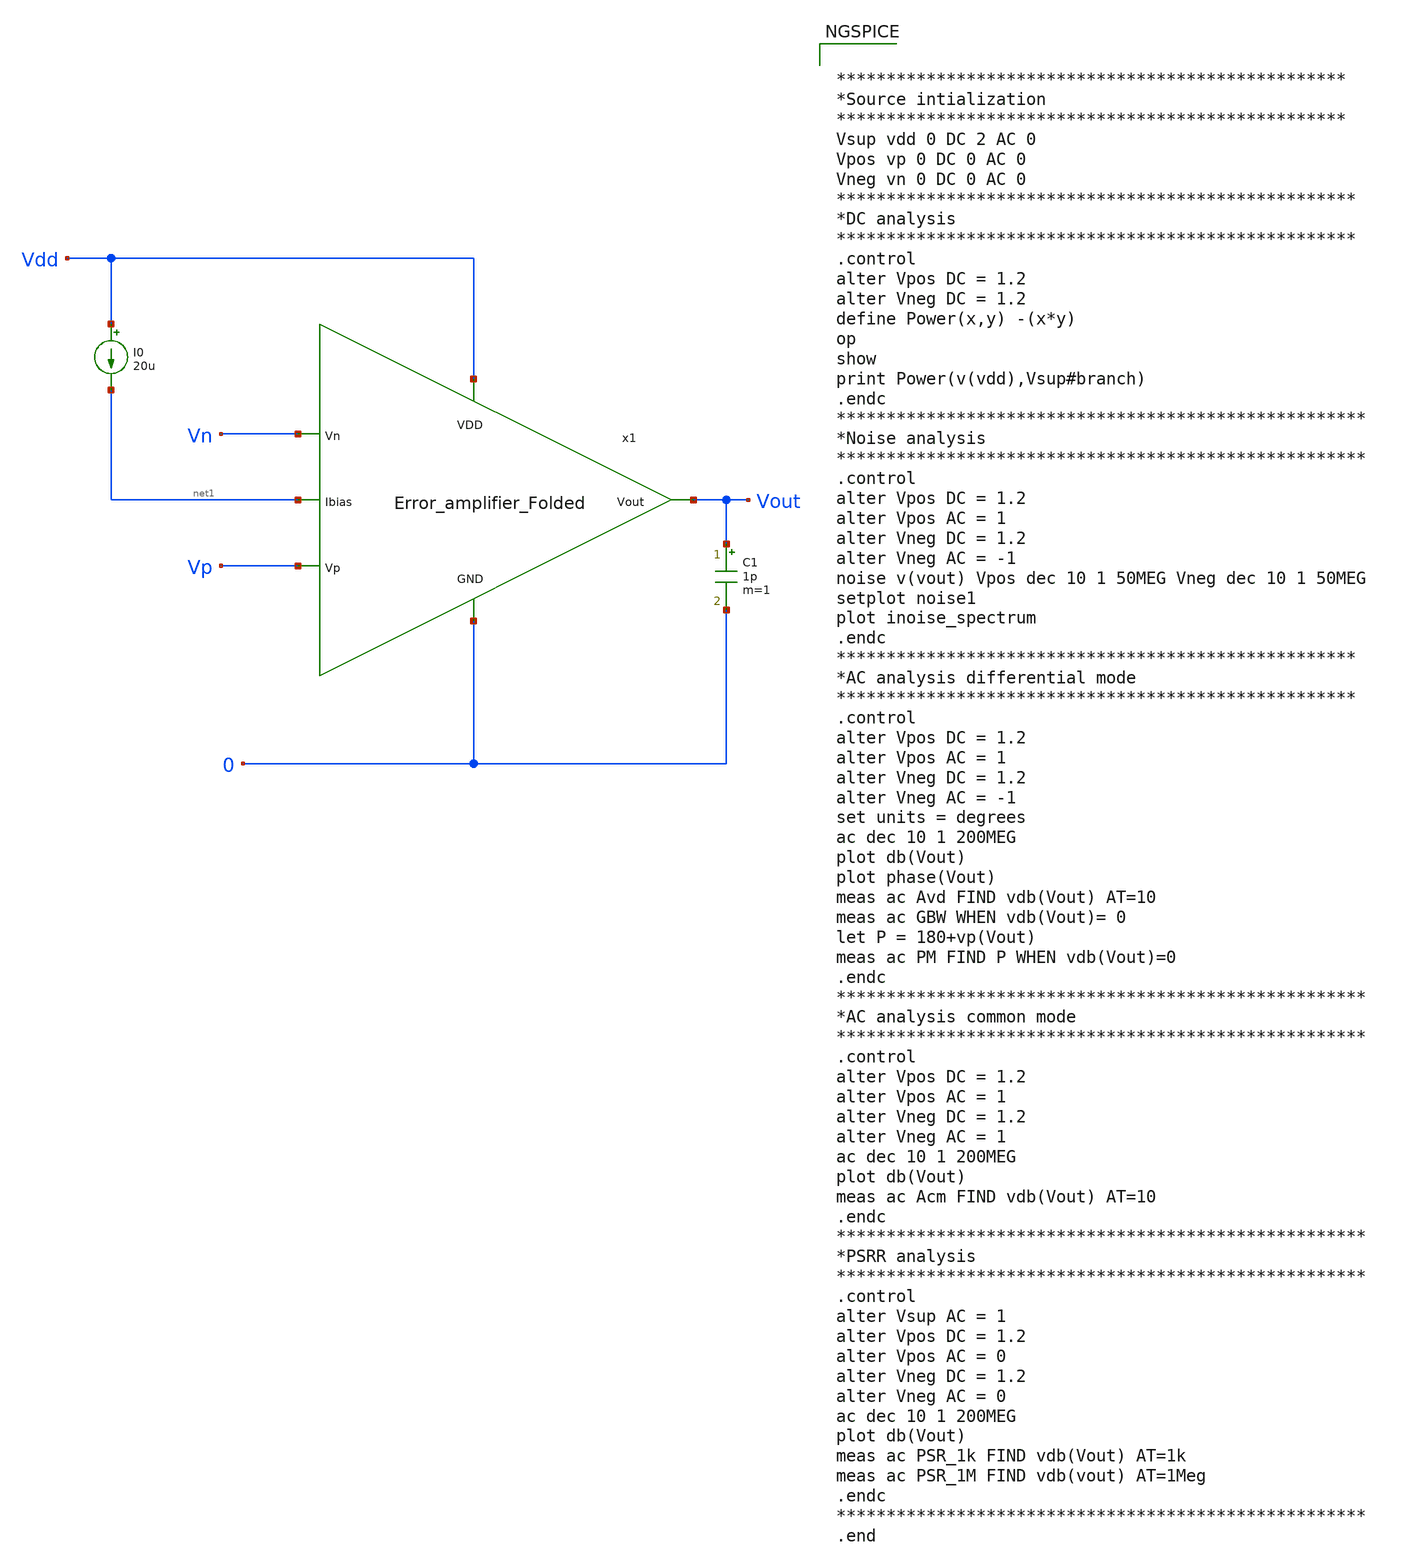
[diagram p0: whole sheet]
** sch_path: Analog_Blocks/OTA/Testbench/Folded_Cascode/Transistor5v/Error_amplifier_Folded_TB.sch
**.subckt Error_amplifier_Folded_TB
I0 Vdd net1 20u
C1 Vout 0 1p m=1
x1 Vdd Vout Vp Vn net1 0 Error_amplifier_Folded
**** begin user architecture code


***************************************************
*Source intialization
***************************************************
Vsup vdd 0 DC 2 AC 0
Vpos vp 0 DC 0 AC 0
Vneg vn 0 DC 0 AC 0
****************************************************
*DC analysis
****************************************************
.control
alter Vpos DC = 1.2
alter Vneg DC = 1.2
define Power(x,y) -(x*y)
op
show
print Power(v(vdd),Vsup#branch)
.endc
*****************************************************
*Noise analysis
*****************************************************
.control
alter Vpos DC = 1.2
alter Vpos AC = 1
alter Vneg DC = 1.2
alter Vneg AC = -1
noise v(vout) Vpos dec 10 1 50MEG Vneg dec 10 1 50MEG
setplot noise1
plot inoise_spectrum
.endc
****************************************************
*AC analysis differential mode
****************************************************
.control
alter Vpos DC = 1.2
alter Vpos AC = 1
alter Vneg DC = 1.2
alter Vneg AC = -1
set units = degrees
ac dec 10 1 200MEG
plot db(Vout)
plot phase(Vout)
meas ac Avd FIND vdb(Vout) AT=10
meas ac GBW WHEN vdb(Vout)= 0
let P = 180+vp(Vout)
meas ac PM FIND P WHEN vdb(Vout)=0
.endc
*****************************************************
*AC analysis common mode
*****************************************************
.control
alter Vpos DC = 1.2
alter Vpos AC = 1
alter Vneg DC = 1.2
alter Vneg AC = 1
ac dec 10 1 200MEG
plot db(Vout)
meas ac Acm FIND vdb(Vout) AT=10
.endc
*****************************************************
*PSRR analysis
*****************************************************
.control
alter Vsup AC = 1
alter Vpos DC = 1.2
alter Vpos AC = 0
alter Vneg DC = 1.2
alter Vneg AC = 0
ac dec 10 1 200MEG
plot db(Vout)
meas ac PSR_1k FIND vdb(Vout) AT=1k
meas ac PSR_1M FIND vdb(vout) AT=1Meg
.endc
*****************************************************
.end




.param mc_mm_switch=0
.param mc_pr_switch=0
.include ~/mabrains/Analog_blocks/models/sky130A/libs.ref/sky130_fd_pr/spice/sky130_fd_pr__nfet_01v8__tt.corner.spice
.include ~/mabrains/Analog_blocks/models/sky130A/libs.ref/sky130_fd_pr/spice/sky130_fd_pr__nfet_01v8_lvt__tt.corner.spice
.include ~/mabrains/Analog_blocks/models/sky130A/libs.ref/sky130_fd_pr/spice/sky130_fd_pr__pfet_01v8__tt.corner.spice
.include ~/mabrains/Analog_blocks/models/sky130A/libs.ref/sky130_fd_pr/spice/sky130_fd_pr__nfet_03v3_nvt__tt.corner.spice
.include ~/mabrains/Analog_blocks/models/sky130A/libs.ref/sky130_fd_pr/spice/sky130_fd_pr__nfet_05v0_nvt__tt.corner.spice
.include ~/mabrains/Analog_blocks/models/sky130A/libs.ref/sky130_fd_pr/spice/sky130_fd_pr__esd_nfet_01v8__tt.corner.spice
.include ~/mabrains/Analog_blocks/models/sky130A/libs.ref/sky130_fd_pr/spice/sky130_fd_pr__pfet_01v8_lvt__tt.corner.spice
.include ~/mabrains/Analog_blocks/models/sky130A/libs.ref/sky130_fd_pr/spice/sky130_fd_pr__pfet_01v8_hvt__tt.corner.spice
.include ~/mabrains/Analog_blocks/models/sky130A/libs.ref/sky130_fd_pr/spice/sky130_fd_pr__esd_pfet_g5v0d10v5__tt.corner.spice
.include ~/mabrains/Analog_blocks/models/sky130A/libs.ref/sky130_fd_pr/spice/sky130_fd_pr__pfet_g5v0d10v5__tt.corner.spice
.include ~/mabrains/Analog_blocks/models/sky130A/libs.ref/sky130_fd_pr/spice/sky130_fd_pr__pfet_g5v0d16v0__tt.corner.spice
.include ~/mabrains/Analog_blocks/models/sky130A/libs.ref/sky130_fd_pr/spice/sky130_fd_pr__nfet_g5v0d10v5__tt.corner.spice
.include ~/mabrains/Analog_blocks/models/sky130A/libs.ref/sky130_fd_pr/spice/sky130_fd_pr__nfet_g5v0d16v0__tt_discrete.corner.spice
.include ~/mabrains/Analog_blocks/models/sky130A/libs.ref/sky130_fd_pr/spice/sky130_fd_pr__esd_nfet_g5v0d10v5__tt.corner.spice
.include ~/mabrains/Analog_blocks/models/sky130A/libs.tech/ngspice/corners/tt/nonfet.spice
* Mismatch parameters
.include ~/mabrains/Analog_blocks/models/sky130A/libs.ref/sky130_fd_pr/spice/sky130_fd_pr__nfet_01v8__mismatch.corner.spice
.include ~/mabrains/Analog_blocks/models/sky130A/libs.ref/sky130_fd_pr/spice/sky130_fd_pr__pfet_01v8__mismatch.corner.spice
.include ~/mabrains/Analog_blocks/models/sky130A/libs.ref/sky130_fd_pr/spice/sky130_fd_pr__nfet_01v8_lvt__mismatch.corner.spice
.include ~/mabrains/Analog_blocks/models/sky130A/libs.ref/sky130_fd_pr/spice/sky130_fd_pr__pfet_01v8_lvt__mismatch.corner.spice
.include ~/mabrains/Analog_blocks/models/sky130A/libs.ref/sky130_fd_pr/spice/sky130_fd_pr__pfet_01v8_hvt__mismatch.corner.spice
.include ~/mabrains/Analog_blocks/models/sky130A/libs.ref/sky130_fd_pr/spice/sky130_fd_pr__nfet_g5v0d10v5__mismatch.corner.spice
.include ~/mabrains/Analog_blocks/models/sky130A/libs.ref/sky130_fd_pr/spice/sky130_fd_pr__pfet_g5v0d10v5__mismatch.corner.spice
.include ~/mabrains/Analog_blocks/models/sky130A/libs.ref/sky130_fd_pr/spice/sky130_fd_pr__nfet_05v0_nvt__mismatch.corner.spice
.include ~/mabrains/Analog_blocks/models/sky130A/libs.ref/sky130_fd_pr/spice/sky130_fd_pr__nfet_03v3_nvt__mismatch.corner.spice
* Resistor/Capacitor
.include ~/mabrains/Analog_blocks/models/sky130A/libs.tech/ngspice/r+c/res_typical__cap_typical.spice
.include ~/mabrains/Analog_blocks/models/sky130A/libs.tech/ngspice/r+c/res_typical__cap_typical__lin.spice
* Special cells
.include ~/mabrains/Analog_blocks/models/sky130A/libs.tech/ngspice/corners/tt/specialized_cells.spice
* All models
.include ~/mabrains/Analog_blocks/models/sky130A/libs.tech/ngspice/all.spice
* Corner
.include ~/mabrains/Analog_blocks/models/sky130A/libs.tech/ngspice/corners/tt/rf.spice



**** end user architecture code
**.ends

* expanding   symbol:
*+  /home/eslam/mabrains/Analog_blocks/Analog_Blocks/LDO/Schematic/LDO_Folded_1.8v/Error_amplifier_Folded.sym # of pins=6
** sym_path: Analog_Blocks/LDO/Schematic/LDO_Folded_1.8v/Error_amplifier_Folded.sym
** sch_path: Analog_Blocks/LDO/Schematic/LDO_Folded_1.8v/Error_amplifier_Folded.sch
.subckt Error_amplifier_Folded VDD Vout Vp Vn Ibias GND
*.ipin VDD
*.ipin GND
*.ipin Vp
*.ipin Vn
*.opin Vout
*.ipin Ibias
XM1 net3 Vp net1 GND sky130_fd_pr__nfet_g5v0d10v5 L=0.5 W=50 nf=1 ad='int((nf+1)/2) * W/nf * 0.29' as='int((nf+2)/2) * W/nf * 0.29'
+ pd='2*int((nf+1)/2) * (W/nf + 0.29)' ps='2*int((nf+2)/2) * (W/nf + 0.29)' nrd='0.29 / W' nrs='0.29 / W'
+ sa=0 sb=0 sd=0 mult=1 m=1
XM2 net2 Vn net1 GND sky130_fd_pr__nfet_g5v0d10v5 L=0.5 W=50 nf=1 ad='int((nf+1)/2) * W/nf * 0.29' as='int((nf+2)/2) * W/nf * 0.29'
+ pd='2*int((nf+1)/2) * (W/nf + 0.29)' ps='2*int((nf+2)/2) * (W/nf + 0.29)' nrd='0.29 / W' nrs='0.29 / W'
+ sa=0 sb=0 sd=0 mult=1 m=1
XM9 Vout net4 GND GND sky130_fd_pr__nfet_g5v0d10v5 L=2 W=6 nf=1 ad='int((nf+1)/2) * W/nf * 0.29' as='int((nf+2)/2) * W/nf * 0.29'
+ pd='2*int((nf+1)/2) * (W/nf + 0.29)' ps='2*int((nf+2)/2) * (W/nf + 0.29)' nrd='0.29 / W' nrs='0.29 / W'
+ sa=0 sb=0 sd=0 mult=1 m=1
XM6 net4 net6 net3 VDD sky130_fd_pr__pfet_g5v0d10v5 L=0.5 W=40 nf=1 ad='int((nf+1)/2) * W/nf * 0.29'
+ as='int((nf+2)/2) * W/nf * 0.29' pd='2*int((nf+1)/2) * (W/nf + 0.29)' ps='2*int((nf+2)/2) * (W/nf + 0.29)'
+ nrd='0.29 / W' nrs='0.29 / W' sa=0 sb=0 sd=0 mult=1 m=1
XM5 net2 net5 VDD VDD sky130_fd_pr__pfet_g5v0d10v5 L=0.5 W=40 nf=1 ad='int((nf+1)/2) * W/nf * 0.29' as='int((nf+2)/2) * W/nf * 0.29'
+ pd='2*int((nf+1)/2) * (W/nf + 0.29)' ps='2*int((nf+2)/2) * (W/nf + 0.29)' nrd='0.29 / W' nrs='0.29 / W'
+ sa=0 sb=0 sd=0 mult=1 m=1
XM4 net3 net5 VDD VDD sky130_fd_pr__pfet_g5v0d10v5 L=0.5 W=40 nf=1 ad='int((nf+1)/2) * W/nf * 0.29' as='int((nf+2)/2) * W/nf * 0.29'
+ pd='2*int((nf+1)/2) * (W/nf + 0.29)' ps='2*int((nf+2)/2) * (W/nf + 0.29)' nrd='0.29 / W' nrs='0.29 / W'
+ sa=0 sb=0 sd=0 mult=1 m=1
XM3 net1 Ibias GND GND sky130_fd_pr__nfet_g5v0d10v5 L=0.9 W=12 nf=1 ad='int((nf+1)/2) * W/nf * 0.29'
+ as='int((nf+2)/2) * W/nf * 0.29' pd='2*int((nf+1)/2) * (W/nf + 0.29)' ps='2*int((nf+2)/2) * (W/nf + 0.29)'
+ nrd='0.29 / W' nrs='0.29 / W' sa=0 sb=0 sd=0 mult=1 m=1
XM7 Vout net6 net2 VDD sky130_fd_pr__pfet_g5v0d10v5 L=0.5 W=40 nf=1 ad='int((nf+1)/2) * W/nf * 0.29'
+ as='int((nf+2)/2) * W/nf * 0.29' pd='2*int((nf+1)/2) * (W/nf + 0.29)' ps='2*int((nf+2)/2) * (W/nf + 0.29)'
+ nrd='0.29 / W' nrs='0.29 / W' sa=0 sb=0 sd=0 mult=1 m=1
XM8 net4 net4 GND GND sky130_fd_pr__nfet_g5v0d10v5 L=2 W=6 nf=1 ad='int((nf+1)/2) * W/nf * 0.29' as='int((nf+2)/2) * W/nf * 0.29'
+ pd='2*int((nf+1)/2) * (W/nf + 0.29)' ps='2*int((nf+2)/2) * (W/nf + 0.29)' nrd='0.29 / W' nrs='0.29 / W'
+ sa=0 sb=0 sd=0 mult=1 m=1
XM10 Ibias Ibias GND GND sky130_fd_pr__nfet_g5v0d10v5 L=0.9 W=12 nf=1 ad='int((nf+1)/2) * W/nf * 0.29'
+ as='int((nf+2)/2) * W/nf * 0.29' pd='2*int((nf+1)/2) * (W/nf + 0.29)' ps='2*int((nf+2)/2) * (W/nf + 0.29)'
+ nrd='0.29 / W' nrs='0.29 / W' sa=0 sb=0 sd=0 mult=1 m=1
XM11 net5 Ibias GND GND sky130_fd_pr__nfet_g5v0d10v5 L=0.9 W=6 nf=1 ad='int((nf+1)/2) * W/nf * 0.29'
+ as='int((nf+2)/2) * W/nf * 0.29' pd='2*int((nf+1)/2) * (W/nf + 0.29)' ps='2*int((nf+2)/2) * (W/nf + 0.29)'
+ nrd='0.29 / W' nrs='0.29 / W' sa=0 sb=0 sd=0 mult=1 m=1
XM12 net6 Ibias GND GND sky130_fd_pr__nfet_g5v0d10v5 L=0.9 W=6 nf=1 ad='int((nf+1)/2) * W/nf * 0.29'
+ as='int((nf+2)/2) * W/nf * 0.29' pd='2*int((nf+1)/2) * (W/nf + 0.29)' ps='2*int((nf+2)/2) * (W/nf + 0.29)'
+ nrd='0.29 / W' nrs='0.29 / W' sa=0 sb=0 sd=0 mult=1 m=1
XM13 net5 net5 VDD VDD sky130_fd_pr__pfet_g5v0d10v5 L=0.5 W=13.5 nf=1 ad='int((nf+1)/2) * W/nf * 0.29'
+ as='int((nf+2)/2) * W/nf * 0.29' pd='2*int((nf+1)/2) * (W/nf + 0.29)' ps='2*int((nf+2)/2) * (W/nf + 0.29)'
+ nrd='0.29 / W' nrs='0.29 / W' sa=0 sb=0 sd=0 mult=1 m=1
XM14 net6 net6 VDD VDD sky130_fd_pr__pfet_g5v0d10v5 L=1 W=2 nf=1 ad='int((nf+1)/2) * W/nf * 0.29' as='int((nf+2)/2) * W/nf * 0.29'
+ pd='2*int((nf+1)/2) * (W/nf + 0.29)' ps='2*int((nf+2)/2) * (W/nf + 0.29)' nrd='0.29 / W' nrs='0.29 / W'
+ sa=0 sb=0 sd=0 mult=1 m=1
.ends

.end
